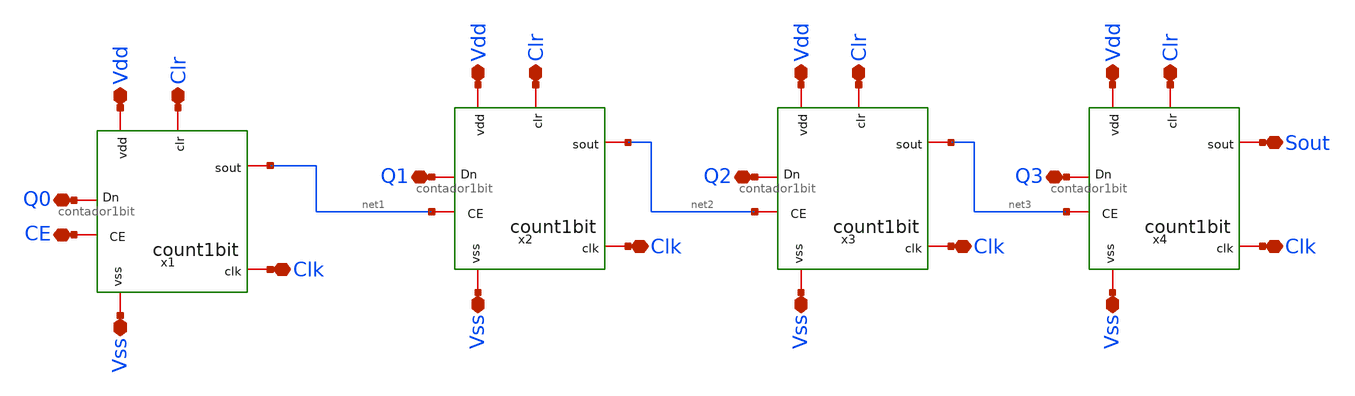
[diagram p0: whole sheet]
** sch_path: design/blocks/circuito_completo/circuito_completo.sch
**.subckt circuito_completo CE Vss Clk Vdd Clr Vss Vdd Clr Clk Vss Vss Clk Clk Clr Clr Vdd Vdd Q0 Q1
*+ Q2 Sout Q3
*.iopin CE
*.iopin Vss
*.iopin Clk
*.iopin Vdd
*.iopin Clr
*.iopin Vss
*.iopin Vdd
*.iopin Clr
*.iopin Clk
*.iopin Vss
*.iopin Vss
*.iopin Clk
*.iopin Clk
*.iopin Clr
*.iopin Clr
*.iopin Vdd
*.iopin Vdd
*.iopin Q0
*.iopin Q1
*.iopin Q2
*.iopin Sout
*.iopin Q3
x1 Clr Q0 CE Clk Vdd Vss net1 contador1bit
x2 Clr Q1 net1 Clk Vdd Vss net2 contador1bit
x3 Clr Q2 net2 Clk Vdd Vss net3 contador1bit
x4 Clr Q3 net3 Clk Vdd Vss Sout contador1bit
**.ends
.end
